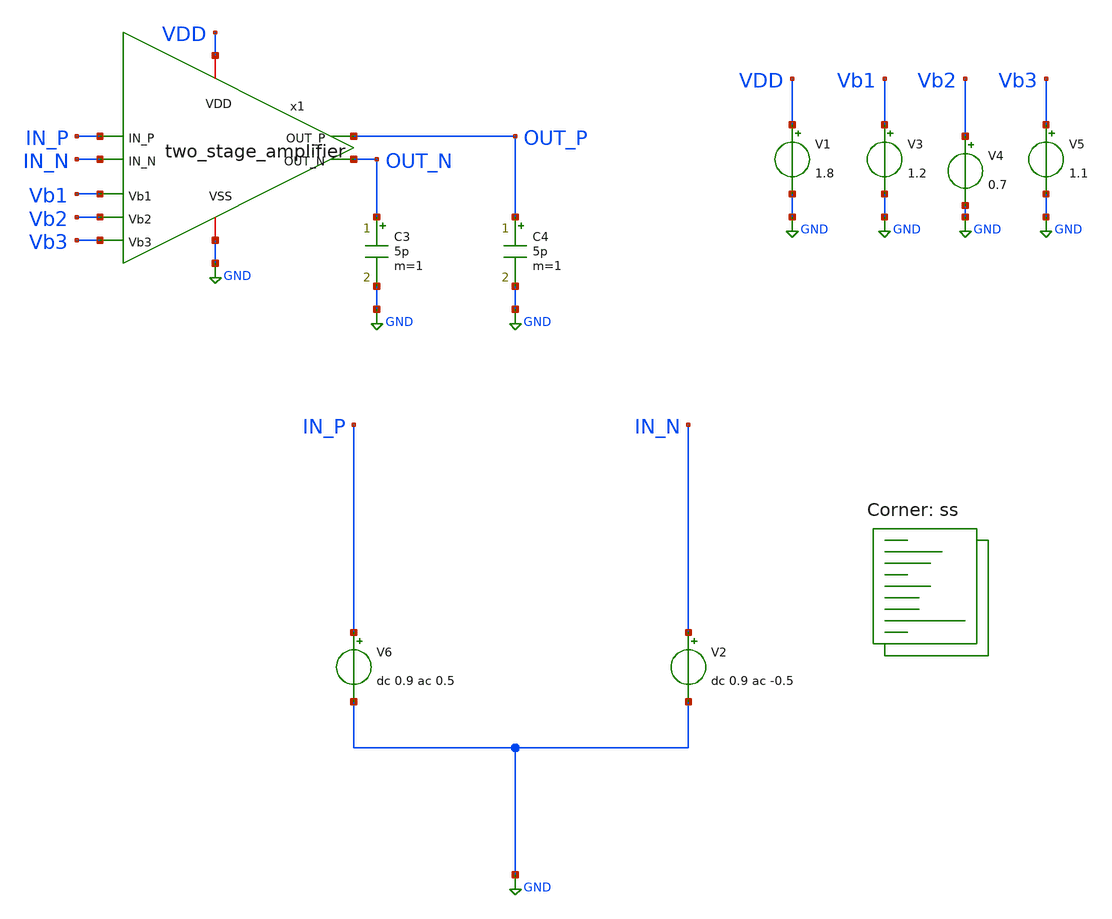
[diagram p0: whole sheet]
** sch_path: xschem/two_stage_amplifier_ac_tb.sch
**.subckt two_stage_amplifier_ac_tb
V1 VDD GND 1.8
.save i(v1)
V3 Vb1 GND 1.2
.save i(v3)
V4 Vb2 GND 0.7
.save i(v4)
V5 Vb3 GND 1.1
.save i(v5)
V6 IN_P GND dc 0.9 ac 0.5
.save i(v6)
x1 VDD Vb3 Vb2 Vb1 IN_P IN_N OUT_P OUT_N GND two_stage_amplifier
C3 OUT_N GND 5p m=1
C4 OUT_P GND 5p m=1
V2 IN_N GND dc 0.9 ac -0.5
.save i(v2)
**** begin user architecture code


.temp 25
.control
option savecurrents
option klu
option method=gear
option noacct
option noinit
save all

save @m.x1.xm1.msky130_fd_pr__nfet_01v8_lvt[gm]
save @m.x1.xm1.msky130_fd_pr__nfet_01v8_lvt[id]
save @m.x1.xm1.msky130_fd_pr__nfet_01v8_lvt[vds]

save @m.x1.xm2.msky130_fd_pr__nfet_01v8_lvt[gm]
save @m.x1.xm2.msky130_fd_pr__nfet_01v8_lvt[id]
save @m.x1.xm2.msky130_fd_pr__nfet_01v8_lvt[vds]

save @m.x1.xm3.msky130_fd_pr__nfet_01v8_lvt[gm]
save @m.x1.xm3.msky130_fd_pr__nfet_01v8_lvt[id]
save @m.x1.xm3.msky130_fd_pr__nfet_01v8_lvt[vds]

save @m.x1.xm4.msky130_fd_pr__nfet_01v8_lvt[gm]
save @m.x1.xm4.msky130_fd_pr__nfet_01v8_lvt[id]
save @m.x1.xm4.msky130_fd_pr__nfet_01v8_lvt[vds]

save @m.x1.xm5.msky130_fd_pr__pfet_01v8_lvt[gm]
save @m.x1.xm5.msky130_fd_pr__pfet_01v8_lvt[id]
save @m.x1.xm5.msky130_fd_pr__pfet_01v8_lvt[vds]

save @m.x1.xm6.msky130_fd_pr__pfet_01v8_lvt[gm]
save @m.x1.xm6.msky130_fd_pr__pfet_01v8_lvt[id]
save @m.x1.xm6.msky130_fd_pr__pfet_01v8_lvt[vds]

save @m.x1.xm7.msky130_fd_pr__pfet_01v8_lvt[gm]
save @m.x1.xm7.msky130_fd_pr__pfet_01v8_lvt[id]
save @m.x1.xm7.msky130_fd_pr__pfet_01v8_lvt[vds]

save @m.x1.xm8.msky130_fd_pr__pfet_01v8_lvt[gm]
save @m.x1.xm8.msky130_fd_pr__pfet_01v8_lvt[id]
save @m.x1.xm8.msky130_fd_pr__pfet_01v8_lvt[vds]

save @m.x1.xm9.msky130_fd_pr__nfet_01v8_lvt[gm]
save @m.x1.xm9.msky130_fd_pr__nfet_01v8_lvt[id]
save @m.x1.xm9.msky130_fd_pr__nfet_01v8_lvt[vds]

save @m.x1.xm10.msky130_fd_pr__nfet_01v8_lvt[gm]
save @m.x1.xm10.msky130_fd_pr__nfet_01v8_lvt[id]
save @m.x1.xm10.msky130_fd_pr__nfet_01v8_lvt[vds]

save @m.x1.xm11.msky130_fd_pr__pfet_01v8_lvt[gm]
save @m.x1.xm11.msky130_fd_pr__pfet_01v8_lvt[id]
save @m.x1.xm11.msky130_fd_pr__pfet_01v8_lvt[vds]

save @m.x1.xm12.msky130_fd_pr__pfet_01v8_lvt[gm]
save @m.x1.xm12.msky130_fd_pr__pfet_01v8_lvt[id]
save @m.x1.xm12.msky130_fd_pr__pfet_01v8_lvt[vds]

save @m.x1.xm13.msky130_fd_pr__nfet_01v8_lvt[gm]
save @m.x1.xm13.msky130_fd_pr__nfet_01v8_lvt[id]
save @m.x1.xm13.msky130_fd_pr__nfet_01v8_lvt[vds]

save @m.x1.xm14.msky130_fd_pr__nfet_01v8_lvt[gm]
save @m.x1.xm14.msky130_fd_pr__nfet_01v8_lvt[id]
save @m.x1.xm14.msky130_fd_pr__nfet_01v8_lvt[vds]

op
write two_stage_amplifier_ac_tb.raw

ac dec 10 1k 10G
let out_gain = db(mag(out_p - out_n))
let out_ph = phase(out_p - out_n) / pi * 180
plot out_gain
plot out_ph
meas ac w_u WHEN out_gain=0
meas ac p_x WHEN out_ph=0
meas ac p_u find out_ph AT=w_u
let w_u_mhz = w_u / 1e6
let phase_mar = 180 + p_u
print w_u_mhz phase_mar
.endc

.lib $::SKYWATER_MODELS/sky130.lib.spice ss
**** end user architecture code
**.ends

* expanding   symbol:  two_stage_amplifier.sym # of pins=9
** sym_path: xschem/two_stage_amplifier.sym
** sch_path: xschem/two_stage_amplifier.sch
.subckt two_stage_amplifier VDD Vb3 Vb2 Vb1 IN_P IN_N OUT_P OUT_N VSS
*.iopin VSS
*.iopin VDD
*.ipin Vb1
*.ipin Vb2
*.ipin Vb3
*.ipin IN_P
*.ipin IN_N
*.opin OUT_N
*.opin OUT_P
XM1 net1 IN_P net3 VSS sky130_fd_pr__nfet_01v8_lvt L=0.3 W=800 nf=1 ad='int((1 + 1)/2) * 800 / 1 * 0.29'
+ as='int((1 + 2)/2) * 800 / 1 * 0.29' pd='2*int((1 + 1)/2) * (800 / 1 + 0.29)' ps='2*int((1 + 2)/2) * (800 / 1 + 0.29)'
+ nrd='0.29 / 800 ' nrs='0.29 / 800 ' sa=0 sb=0 sd=0 mult=1 m=1
XM2 net2 IN_N net3 VSS sky130_fd_pr__nfet_01v8_lvt L=0.3 W=800 nf=1 ad='int((1 + 1)/2) * 800 / 1 * 0.29'
+ as='int((1 + 2)/2) * 800 / 1 * 0.29' pd='2*int((1 + 1)/2) * (800 / 1 + 0.29)' ps='2*int((1 + 2)/2) * (800 / 1 + 0.29)'
+ nrd='0.29 / 800 ' nrs='0.29 / 800 ' sa=0 sb=0 sd=0 mult=1 m=1
XM3 T_OUT_N Vb1 net1 VSS sky130_fd_pr__nfet_01v8_lvt L=0.3 W=800 nf=1 ad='int((1 + 1)/2) * 800 / 1 * 0.29'
+ as='int((1 + 2)/2) * 800 / 1 * 0.29' pd='2*int((1 + 1)/2) * (800 / 1 + 0.29)' ps='2*int((1 + 2)/2) * (800 / 1 + 0.29)'
+ nrd='0.29 / 800 ' nrs='0.29 / 800 ' sa=0 sb=0 sd=0 mult=1 m=1
XM4 T_OUT_P Vb1 net2 VSS sky130_fd_pr__nfet_01v8_lvt L=0.3 W=800 nf=1 ad='int((1 + 1)/2) * 800 / 1 * 0.29'
+ as='int((1 + 2)/2) * 800 / 1 * 0.29' pd='2*int((1 + 1)/2) * (800 / 1 + 0.29)' ps='2*int((1 + 2)/2) * (800 / 1 + 0.29)'
+ nrd='0.29 / 800 ' nrs='0.29 / 800 ' sa=0 sb=0 sd=0 mult=1 m=1
XM5 T_OUT_N Vb2 net4 net4 sky130_fd_pr__pfet_01v8_lvt L=0.8 W=600 nf=1 ad='int((1 + 1)/2) * 600 / 1 * 0.29'
+ as='int((1 + 2)/2) * 600 / 1 * 0.29' pd='2*int((1 + 1)/2) * (600 / 1 + 0.29)' ps='2*int((1 + 2)/2) * (600 / 1 + 0.29)'
+ nrd='0.29 / 600 ' nrs='0.29 / 600 ' sa=0 sb=0 sd=0 mult=1 m=1
XM6 T_OUT_P Vb2 net5 net5 sky130_fd_pr__pfet_01v8_lvt L=0.8 W=600 nf=1 ad='int((1 + 1)/2) * 600 / 1 * 0.29'
+ as='int((1 + 2)/2) * 600 / 1 * 0.29' pd='2*int((1 + 1)/2) * (600 / 1 + 0.29)' ps='2*int((1 + 2)/2) * (600 / 1 + 0.29)'
+ nrd='0.29 / 600 ' nrs='0.29 / 600 ' sa=0 sb=0 sd=0 mult=1 m=1
XM7 net4 Vb3 VDD VDD sky130_fd_pr__pfet_01v8_lvt L=0.8 W=600 nf=1 ad='int((1 + 1)/2) * 600 / 1 * 0.29'
+ as='int((1 + 2)/2) * 600 / 1 * 0.29' pd='2*int((1 + 1)/2) * (600 / 1 + 0.29)' ps='2*int((1 + 2)/2) * (600 / 1 + 0.29)'
+ nrd='0.29 / 600 ' nrs='0.29 / 600 ' sa=0 sb=0 sd=0 mult=1 m=1
XM8 net5 Vb3 VDD VDD sky130_fd_pr__pfet_01v8_lvt L=0.8 W=600 nf=1 ad='int((1 + 1)/2) * 600 / 1 * 0.29'
+ as='int((1 + 2)/2) * 600 / 1 * 0.29' pd='2*int((1 + 1)/2) * (600 / 1 + 0.29)' ps='2*int((1 + 2)/2) * (600 / 1 + 0.29)'
+ nrd='0.29 / 600 ' nrs='0.29 / 600 ' sa=0 sb=0 sd=0 mult=1 m=1
XM9 net3 T_OUT_N VSS VSS sky130_fd_pr__nfet_01v8_lvt L=0.3 W=25 nf=1 ad='int((1 + 1)/2) * 25 / 1 * 0.29'
+ as='int((1 + 2)/2) * 25 / 1 * 0.29' pd='2*int((1 + 1)/2) * (25 / 1 + 0.29)' ps='2*int((1 + 2)/2) * (25 / 1 + 0.29)'
+ nrd='0.29 / 25 ' nrs='0.29 / 25 ' sa=0 sb=0 sd=0 mult=1 m=1
XM10 net3 T_OUT_P VSS VSS sky130_fd_pr__nfet_01v8_lvt L=0.3 W=25 nf=1 ad='int((1 + 1)/2) * 25 / 1 * 0.29'
+ as='int((1 + 2)/2) * 25 / 1 * 0.29' pd='2*int((1 + 1)/2) * (25 / 1 + 0.29)' ps='2*int((1 + 2)/2) * (25 / 1 + 0.29)'
+ nrd='0.29 / 25 ' nrs='0.29 / 25 ' sa=0 sb=0 sd=0 mult=1 m=1
XM12 OUT_N T_OUT_P VDD VDD sky130_fd_pr__pfet_01v8_lvt L=0.35 W=1000 nf=1 ad='int((1 + 1)/2) * 1000 / 1 * 0.29'
+ as='int((1 + 2)/2) * 1000 / 1 * 0.29' pd='2*int((1 + 1)/2) * (1000 / 1 + 0.29)' ps='2*int((1 + 2)/2) * (1000 / 1 + 0.29)'
+ nrd='0.29 / 1000 ' nrs='0.29 / 1000 ' sa=0 sb=0 sd=0 mult=1 m=1
XM11 OUT_P T_OUT_N VDD VDD sky130_fd_pr__pfet_01v8_lvt L=0.35 W=1000 nf=1 ad='int((1 + 1)/2) * 1000 / 1 * 0.29'
+ as='int((1 + 2)/2) * 1000 / 1 * 0.29' pd='2*int((1 + 1)/2) * (1000 / 1 + 0.29)' ps='2*int((1 + 2)/2) * (1000 / 1 + 0.29)'
+ nrd='0.29 / 1000 ' nrs='0.29 / 1000 ' sa=0 sb=0 sd=0 mult=1 m=1
XM14 OUT_N net6 VSS VSS sky130_fd_pr__nfet_01v8_lvt L=0.35 W=500 nf=1 ad='int((1 + 1)/2) * 500 / 1 * 0.29'
+ as='int((1 + 2)/2) * 500 / 1 * 0.29' pd='2*int((1 + 1)/2) * (500 / 1 + 0.29)' ps='2*int((1 + 2)/2) * (500 / 1 + 0.29)'
+ nrd='0.29 / 500 ' nrs='0.29 / 500 ' sa=0 sb=0 sd=0 mult=1 m=1
XM13 OUT_P net6 VSS VSS sky130_fd_pr__nfet_01v8_lvt L=0.35 W=500 nf=1 ad='int((1 + 1)/2) * 500 / 1 * 0.29'
+ as='int((1 + 2)/2) * 500 / 1 * 0.29' pd='2*int((1 + 1)/2) * (500 / 1 + 0.29)' ps='2*int((1 + 2)/2) * (500 / 1 + 0.29)'
+ nrd='0.29 / 500 ' nrs='0.29 / 500 ' sa=0 sb=0 sd=0 mult=1 m=1
R6 OUT_P net6 1e6 m=1
R7 OUT_N net6 1e6 m=1
XR10 OUT_P net7 sky130_fd_pr__res_generic_po W=1.3 L=1 m=1
XR9 net8 OUT_N sky130_fd_pr__res_generic_po W=1.3 L=1 m=1
XC2 T_OUT_N net7 sky130_fd_pr__cap_mim_m3_1 W=54.6 L=54.6 MF=1 m=1
XC1 T_OUT_P net8 sky130_fd_pr__cap_mim_m3_1 W=54.6 L=54.6 MF=1 m=1
.ends

.GLOBAL GND
.end
